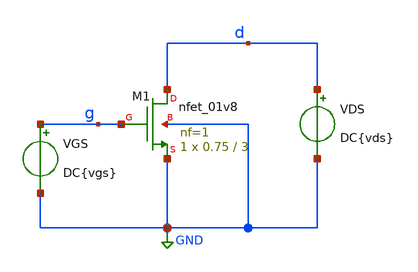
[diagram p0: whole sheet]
** sch_path: icdesign/sch/NMOS/Ej1.sch
**.subckt Ej1
XM1 d g GND GND sky130_fd_pr__nfet_01v8 L=3 W=0.75 nf=1 ad='int((nf+1)/2) * W/nf * 0.29' as='int((nf+2)/2) * W/nf * 0.29'
+ pd='2*int((nf+1)/2) * (W/nf + 0.29)' ps='2*int((nf+2)/2) * (W/nf + 0.29)' nrd='0.29 / W' nrs='0.29 / W'
+ sa=0 sb=0 sd=0 mult=1 m=1
VGS g GND DC{vgs}
VDS d GND DC{vds}
**** begin user architecture code



* Parameters
.param vds = 1.8
.param vgs = 0.9
.options TEMPS = 27.0

* Models
.lib ~/skywater/skywater-pdk/libraries/sky130_fd_pr_ngspice/latest/models/corners/sky130.lib TT

* Data to save
.save all  @M.XM1.msky130_fd_pr__nfet_01v8[id]  @M.XM1.msky130_fd_pr__nfet_01v8[gm]  @M.XM1.msky130_fd_pr__nfet_01v8[vth]  @M.XM1.msky130_fd_pr__nfet_01v8[vds]  @M.XM1.msky130_fd_pr__nfet_01v8[vdsat]  @M.XM1.msky130_fd_pr__nfet_01v8[vgs]


* Simulation
.control
  dc VDS 0 1.8 0.01 VGS 0 1.8 0.3
  setplot dc1
  plot @M.XM1.msky130_fd_pr__nfet_01v8[id] ylabel Id xlabel Vds title 'Id vs Vds vs Vgs'
  set filetype = ascii
  write tp1_1_dc1.raw
.endc
.end


**** end user architecture code
**.ends
.GLOBAL GND
.end
